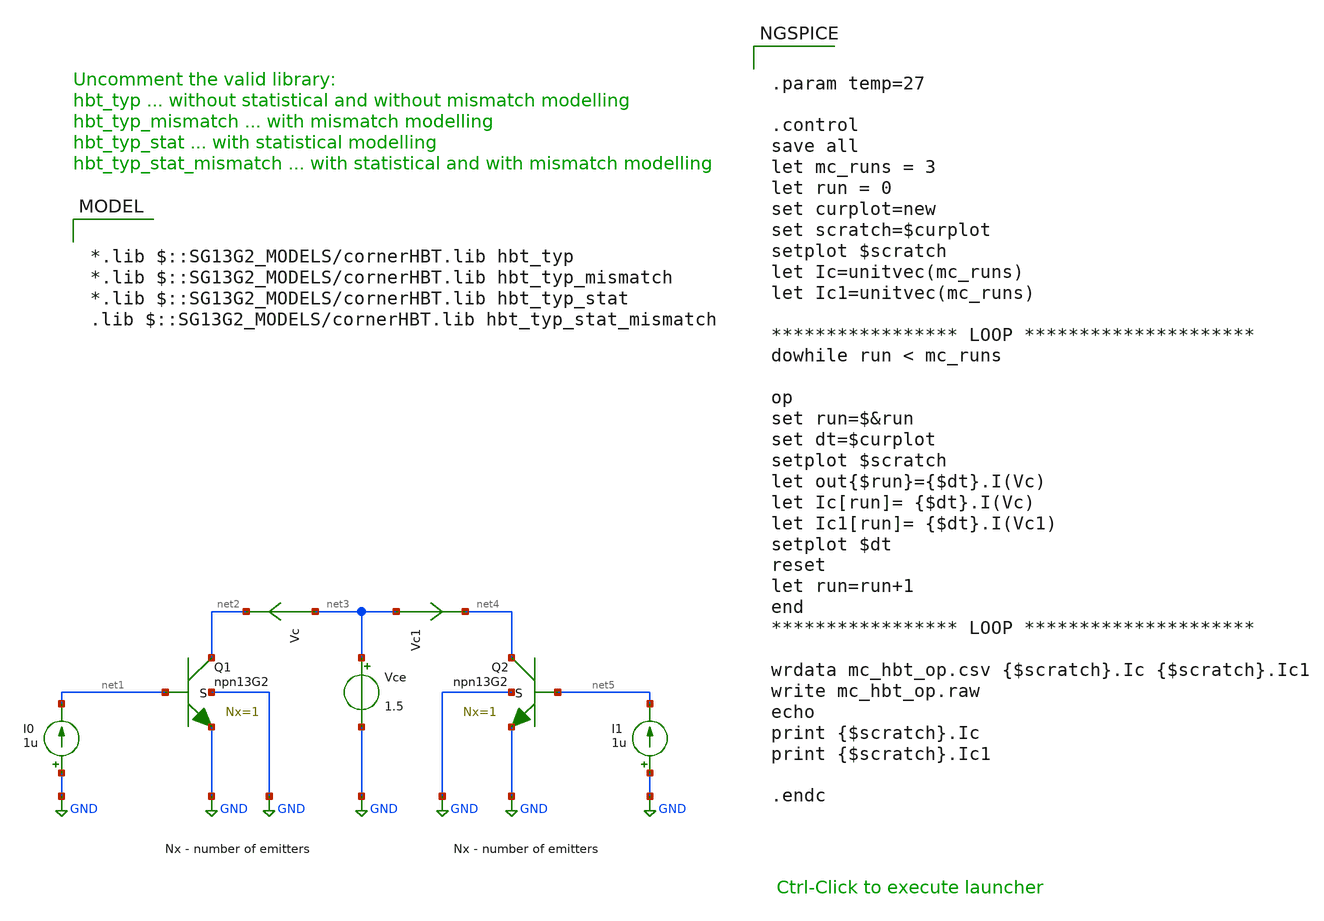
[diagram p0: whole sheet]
** sch_path: ihp-sg13g2/libs.tech/xschem/sg13g2_tests/mc_hbt_13g2.sch
* Copyright 2023 IHP PDK Authors
**.subckt mc_hbt_13g2
Vce net3 GND 1.5
I0 GND net1 1u
Vc net3 net2 0
.save i(vc)
XQ1 net2 net1 GND GND npn13G2 Nx=1 mm_ok=1
XQ2 net4 net5 GND GND npn13G2 Nx=1 mm_ok=1
Vc1 net3 net4 0
.save i(vc1)
I1 GND net5 1u
**** begin user architecture code

*.lib $::SG13G2_MODELS/cornerHBT.lib hbt_typ
*.lib $::SG13G2_MODELS/cornerHBT.lib hbt_typ_mismatch
*.lib $::SG13G2_MODELS/cornerHBT.lib hbt_typ_stat
.lib $::SG13G2_MODELS/cornerHBT.lib hbt_typ_stat_mismatch



.param temp=27

.control
save all
let mc_runs = 3
let run = 0
set curplot=new
set scratch=$curplot
setplot $scratch
let Ic=unitvec(mc_runs)
let Ic1=unitvec(mc_runs)

***************** LOOP *********************
dowhile run < mc_runs

op
set run=$&run
set dt=$curplot
setplot $scratch
let out{$run}={$dt}.I(Vc)
let Ic[run]= {$dt}.I(Vc)
let Ic1[run]= {$dt}.I(Vc1)
setplot $dt
reset
let run=run+1
end
***************** LOOP *********************

wrdata mc_hbt_op.csv {$scratch}.Ic {$scratch}.Ic1
write mc_hbt_op.raw
echo
print {$scratch}.Ic
print {$scratch}.Ic1

.endc


**** end user architecture code
**.ends
.GLOBAL GND
.end
